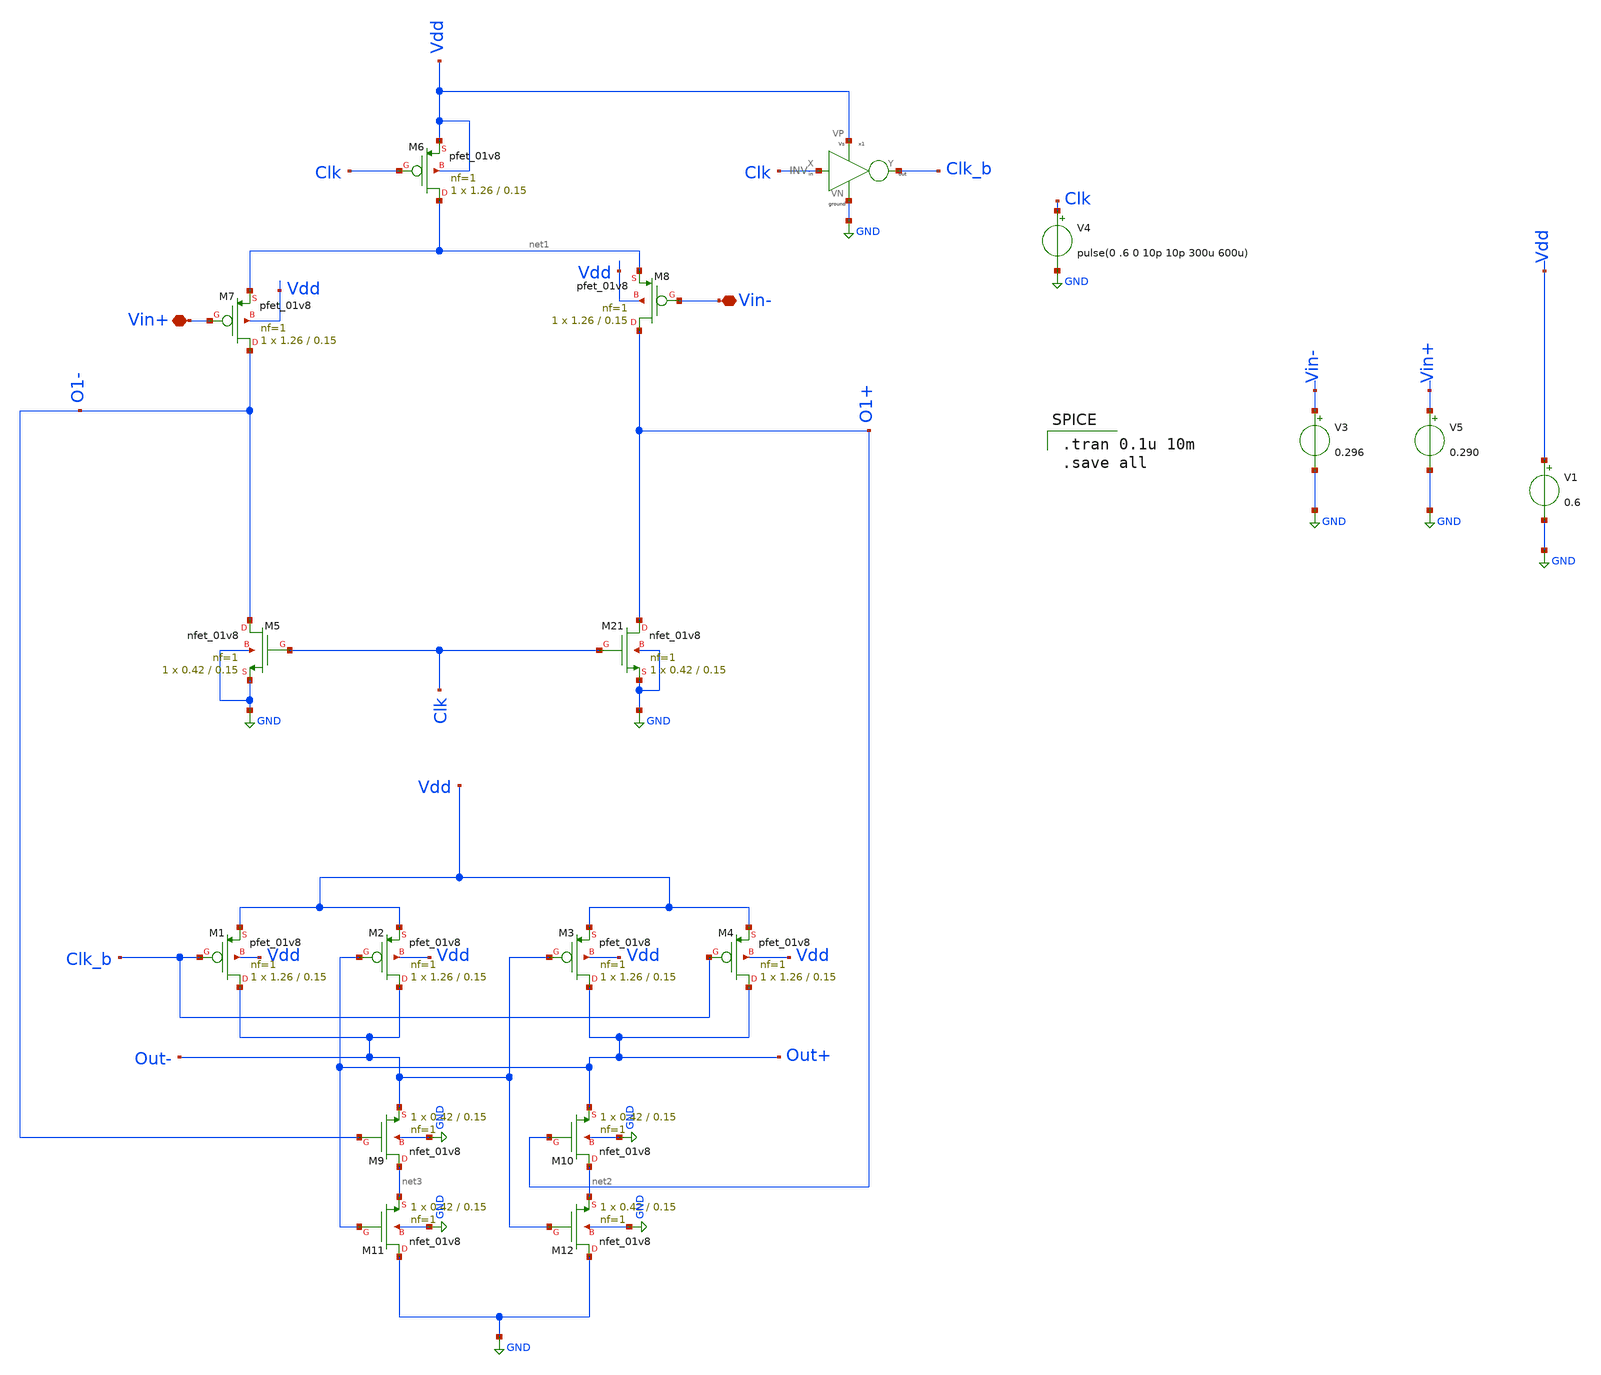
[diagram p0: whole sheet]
** sch_path: untitled-10.sch
**.subckt untitled-10 Vin+ Vin-
*.iopin Vin+
*.iopin Vin-
XM6 net1 Clk Vdd Vdd sky130_fd_pr__pfet_01v8 L=0.15 W=1.26 nf=1 ad='int((nf+1)/2) * W/nf * 0.29' as='int((nf+2)/2) * W/nf * 0.29'
+ pd='2*int((nf+1)/2) * (W/nf + 0.29)' ps='2*int((nf+2)/2) * (W/nf + 0.29)' nrd='0.29 / W' nrs='0.29 / W'
+ sa=0 sb=0 sd=0 mult=1 m=1
XM7 O1- Vin+ net1 Vdd sky130_fd_pr__pfet_01v8 L=0.15 W=1.26 nf=1 ad='int((nf+1)/2) * W/nf * 0.29' as='int((nf+2)/2) * W/nf * 0.29'
+ pd='2*int((nf+1)/2) * (W/nf + 0.29)' ps='2*int((nf+2)/2) * (W/nf + 0.29)' nrd='0.29 / W' nrs='0.29 / W'
+ sa=0 sb=0 sd=0 mult=1 m=1
XM8 O1+ Vin- net1 Vdd sky130_fd_pr__pfet_01v8 L=0.15 W=1.26 nf=1 ad='int((nf+1)/2) * W/nf * 0.29' as='int((nf+2)/2) * W/nf * 0.29'
+ pd='2*int((nf+1)/2) * (W/nf + 0.29)' ps='2*int((nf+2)/2) * (W/nf + 0.29)' nrd='0.29 / W' nrs='0.29 / W'
+ sa=0 sb=0 sd=0 mult=1 m=1
XM5 O1- Clk GND GND sky130_fd_pr__nfet_01v8 L=0.15 W=0.42 nf=1 ad='int((nf+1)/2) * W/nf * 0.29' as='int((nf+2)/2) * W/nf * 0.29'
+ pd='2*int((nf+1)/2) * (W/nf + 0.29)' ps='2*int((nf+2)/2) * (W/nf + 0.29)' nrd='0.29 / W' nrs='0.29 / W'
+ sa=0 sb=0 sd=0 mult=1 m=1
XM21 O1+ Clk GND GND sky130_fd_pr__nfet_01v8 L=0.15 W=0.42 nf=1 ad='int((nf+1)/2) * W/nf * 0.29' as='int((nf+2)/2) * W/nf * 0.29'
+ pd='2*int((nf+1)/2) * (W/nf + 0.29)' ps='2*int((nf+2)/2) * (W/nf + 0.29)' nrd='0.29 / W' nrs='0.29 / W'
+ sa=0 sb=0 sd=0 mult=1 m=1
XM1 Out- Clk_b Vdd Vdd sky130_fd_pr__pfet_01v8 L=0.15 W=1.26 nf=1 ad='int((nf+1)/2) * W/nf * 0.29' as='int((nf+2)/2) * W/nf * 0.29'
+ pd='2*int((nf+1)/2) * (W/nf + 0.29)' ps='2*int((nf+2)/2) * (W/nf + 0.29)' nrd='0.29 / W' nrs='0.29 / W'
+ sa=0 sb=0 sd=0 mult=1 m=1
XM2 Out- Out+ Vdd Vdd sky130_fd_pr__pfet_01v8 L=0.15 W=1.26 nf=1 ad='int((nf+1)/2) * W/nf * 0.29' as='int((nf+2)/2) * W/nf * 0.29'
+ pd='2*int((nf+1)/2) * (W/nf + 0.29)' ps='2*int((nf+2)/2) * (W/nf + 0.29)' nrd='0.29 / W' nrs='0.29 / W'
+ sa=0 sb=0 sd=0 mult=1 m=1
XM3 Out+ Out- Vdd Vdd sky130_fd_pr__pfet_01v8 L=0.15 W=1.26 nf=1 ad='int((nf+1)/2) * W/nf * 0.29' as='int((nf+2)/2) * W/nf * 0.29'
+ pd='2*int((nf+1)/2) * (W/nf + 0.29)' ps='2*int((nf+2)/2) * (W/nf + 0.29)' nrd='0.29 / W' nrs='0.29 / W'
+ sa=0 sb=0 sd=0 mult=1 m=1
XM4 Out+ Clk_b Vdd Vdd sky130_fd_pr__pfet_01v8 L=0.15 W=1.26 nf=1 ad='int((nf+1)/2) * W/nf * 0.29' as='int((nf+2)/2) * W/nf * 0.29'
+ pd='2*int((nf+1)/2) * (W/nf + 0.29)' ps='2*int((nf+2)/2) * (W/nf + 0.29)' nrd='0.29 / W' nrs='0.29 / W'
+ sa=0 sb=0 sd=0 mult=1 m=1
XM9 net3 O1- Out- GND sky130_fd_pr__nfet_01v8 L=0.15 W=0.42 nf=1 ad='int((nf+1)/2) * W/nf * 0.29' as='int((nf+2)/2) * W/nf * 0.29'
+ pd='2*int((nf+1)/2) * (W/nf + 0.29)' ps='2*int((nf+2)/2) * (W/nf + 0.29)' nrd='0.29 / W' nrs='0.29 / W'
+ sa=0 sb=0 sd=0 mult=1 m=1
XM10 net2 O1+ Out+ GND sky130_fd_pr__nfet_01v8 L=0.15 W=0.42 nf=1 ad='int((nf+1)/2) * W/nf * 0.29' as='int((nf+2)/2) * W/nf * 0.29'
+ pd='2*int((nf+1)/2) * (W/nf + 0.29)' ps='2*int((nf+2)/2) * (W/nf + 0.29)' nrd='0.29 / W' nrs='0.29 / W'
+ sa=0 sb=0 sd=0 mult=1 m=1
XM11 GND Out+ net3 GND sky130_fd_pr__nfet_01v8 L=0.15 W=0.42 nf=1 ad='int((nf+1)/2) * W/nf * 0.29' as='int((nf+2)/2) * W/nf * 0.29'
+ pd='2*int((nf+1)/2) * (W/nf + 0.29)' ps='2*int((nf+2)/2) * (W/nf + 0.29)' nrd='0.29 / W' nrs='0.29 / W'
+ sa=0 sb=0 sd=0 mult=1 m=1
XM12 GND Out- net2 GND sky130_fd_pr__nfet_01v8 L=0.15 W=0.42 nf=1 ad='int((nf+1)/2) * W/nf * 0.29' as='int((nf+2)/2) * W/nf * 0.29'
+ pd='2*int((nf+1)/2) * (W/nf + 0.29)' ps='2*int((nf+2)/2) * (W/nf + 0.29)' nrd='0.29 / W' nrs='0.29 / W'
+ sa=0 sb=0 sd=0 mult=1 m=1
x1 Clk Clk_b Vdd GND INV
V3 Vin- GND 0.296
V5 Vin+ GND 0.290
V1 Vdd GND 0.6
V4 Clk GND pulse(0 .6 0 10p 10p 300u 600u)
**** begin user architecture code

** opencircuitdesign pdks install
.lib $::SKYWATER_MODELS/sky130.lib.spice tt



.tran 0.1u 10m
.save all

**** end user architecture code
**.ends

* expanding   symbol:  component/INV/INV.sym # of pins=4
** sym_path: component/INV/INV.sym
** sch_path: component/INV/INV.sch
.subckt INV X Y VP VN
*.ipin X
*.opin Y
*.iopin VN
*.iopin VP
XM1 Y X VN VN sky130_fd_pr__nfet_01v8 L=0.15 W=0.42 nf=1 ad='int((nf+1)/2) * W/nf * 0.29' as='int((nf+2)/2) * W/nf * 0.29'
+ pd='2*int((nf+1)/2) * (W/nf + 0.29)' ps='2*int((nf+2)/2) * (W/nf + 0.29)' nrd='0.29 / W' nrs='0.29 / W'
+ sa=0 sb=0 sd=0 mult=1 m=1
XM2 Y X VP VP sky130_fd_pr__pfet_01v8 L=0.15 W=1.26 nf=1 ad='int((nf+1)/2) * W/nf * 0.29' as='int((nf+2)/2) * W/nf * 0.29'
+ pd='2*int((nf+1)/2) * (W/nf + 0.29)' ps='2*int((nf+2)/2) * (W/nf + 0.29)' nrd='0.29 / W' nrs='0.29 / W'
+ sa=0 sb=0 sd=0 mult=1 m=1
.ends

.GLOBAL GND
.end
